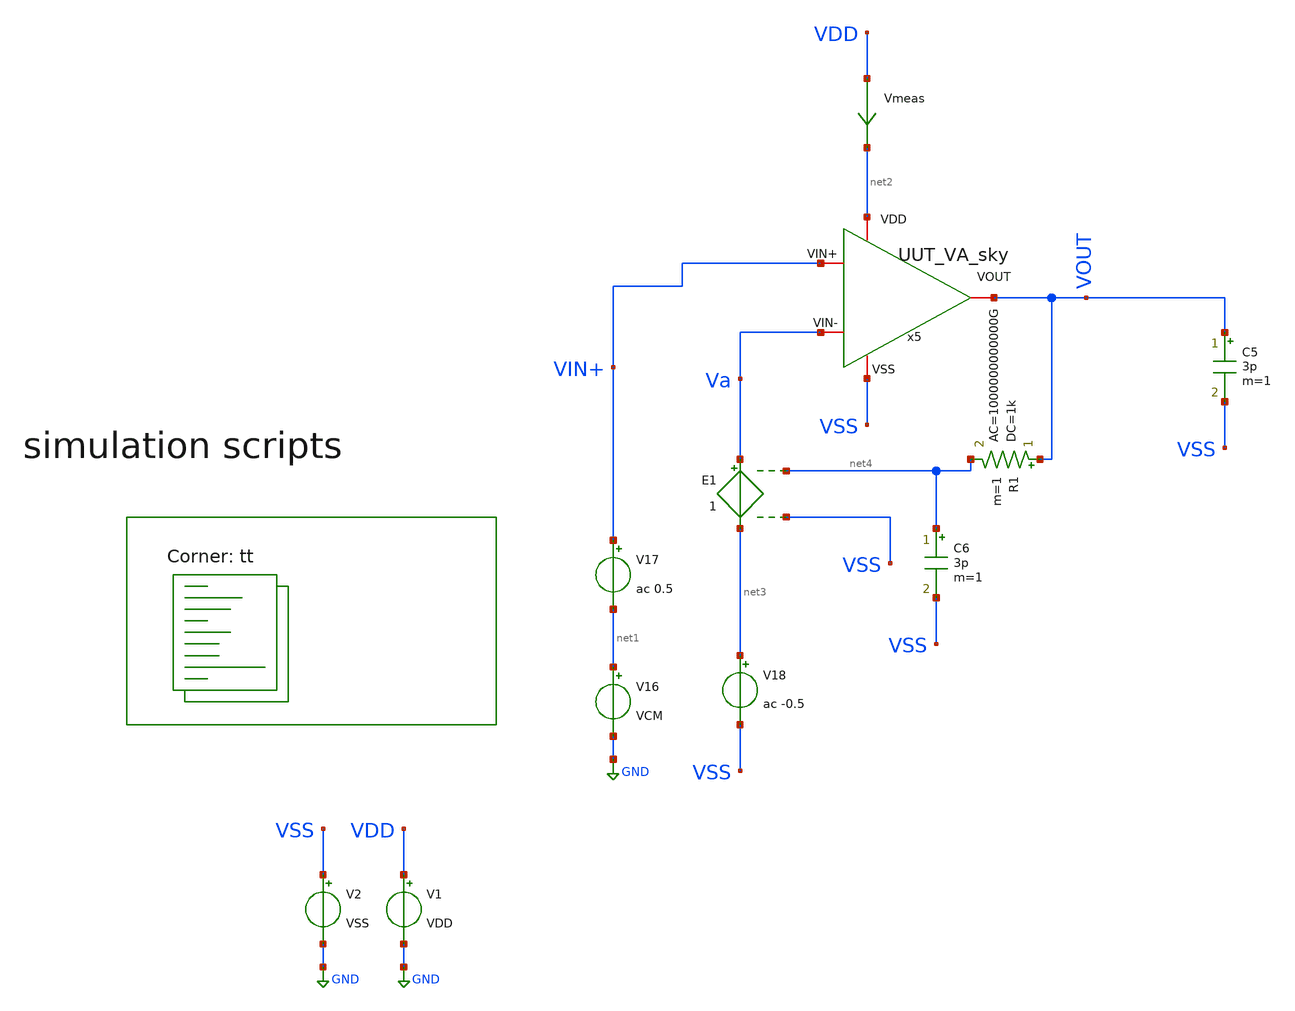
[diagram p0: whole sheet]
** sch_path: Learning/single_ended_amplifiers/VA001_series/Design_and_Analysis_of_Two-Stage_CMOS_Operational_Amplifier_for_Fluorescence_Signal_Processing_sky130_5V/amplifier_design/pz.sch
**.subckt pz
V1 VDD GND VDD
V2 VSS GND VSS
Vmeas VDD net2 0
.save i(vmeas)
x5 net2 VSS Va VIN+ VOUT UUT_VA_sky
C5 VOUT VSS 3p m=1
V16 net1 GND VCM
V17 VIN+ net1 ac 0.5
V18 net3 VSS ac -0.5
E1 Va net3 net4 VSS 1
R1 VOUT net4 1k ac=1000000000000G m=1
C6 net4 VSS 3p m=1
**** begin user architecture code
.lib $::SKYWATER_MODELS/sky130.lib.spice tt

.Temp 27
.param VDD = 5
.param VSS = 0
.param CL = 3p
.param V_OFF = -889u
.param VCM=2.5


.control
	save all
	ac dec 100 1 10G
	plot db(v(VOUT)) (180+(180*ph(v(VOUT))/pi))
	pz VIN+ 0 0 VOUT vol pz
	print all
.endc




**** end user architecture code
**.ends

* expanding   symbol:  Sky130A/UUT_sky/UUT_VA_sky.sym # of pins=5
** sym_path: my_ip/LIB/Sky130A/UUT_sky/UUT_VA_sky.sym
** sch_path: my_ip/LIB/Sky130A/UUT_sky/UUT_VA_sky.sch
.subckt UUT_VA_sky VDD VSS VIN- VIN+ VOUT
*.iopin VDD
*.iopin VSS
*.iopin VIN-
*.iopin VIN+
*.iopin VOUT
x1 VDD VSS VIN+ VIN- VOUT amplifier
.ends


* expanding   symbol:
*+  Sky130A/Learning/Design_of_Two-Stage_CMOS_Operational_Amplifier_for_Fluorescence_Signal_Processing_5V/amplifier.sym # of pins=5
** sym_path: my_ip/LIB/Sky130A/Learning/Design_of_Two-Stage_CMOS_Operational_Amplifier_for_Fluorescence_Signal_Processing_5V/amplifier.sym
** sch_path: my_ip/LIB/Sky130A/Learning/Design_of_Two-Stage_CMOS_Operational_Amplifier_for_Fluorescence_Signal_Processing_5V/amplifier.sch
.subckt amplifier VDD VSS Vin+ Vin- VOUT
*.iopin VDD
*.iopin VSS
*.iopin Vin+
*.iopin Vin-
*.iopin VOUT
XR2 VSS net2 VSS sky130_fd_pr__res_high_po_0p35 L=20.4 mult=1 m=1
XM7 net1 net1 VSS VSS sky130_fd_pr__nfet_g5v0d10v5 L=3.2 W='1 * 2 ' nf=2 ad='int((nf+1)/2) * W / nf * 0.29'
+ as='int((nf+2)/2) * W / nf * 0.29' pd='2*int((nf+1)/2) * (W / nf + 0.29)' ps='2*int((nf+2)/2) * (W / nf + 0.29)'
+ nrd='0.29 / W ' nrs='0.29 / W ' sa=0 sb=0 sd=0 mult=2 m=2
XM8 net3 net1 net2 VSS sky130_fd_pr__nfet_g5v0d10v5 L=3.2 W='1 * 8 ' nf=8 ad='int((nf+1)/2) * W / nf * 0.29'
+ as='int((nf+2)/2) * W / nf * 0.29' pd='2*int((nf+1)/2) * (W / nf + 0.29)' ps='2*int((nf+2)/2) * (W / nf + 0.29)'
+ nrd='0.29 / W ' nrs='0.29 / W ' sa=0 sb=0 sd=0 mult=2 m=2
XM9 VB1 VB2 net3 VSS sky130_fd_pr__nfet_g5v0d10v5 L=2 W='1 * 2 ' nf=2 ad='int((nf+1)/2) * W / nf * 0.29'
+ as='int((nf+2)/2) * W / nf * 0.29' pd='2*int((nf+1)/2) * (W / nf + 0.29)' ps='2*int((nf+2)/2) * (W / nf + 0.29)'
+ nrd='0.29 / W ' nrs='0.29 / W ' sa=0 sb=0 sd=0 mult=2 m=2
XM10 VB2 VB2 net1 VSS sky130_fd_pr__nfet_g5v0d10v5 L=2 W='1 * 2 ' nf=2 ad='int((nf+1)/2) * W / nf * 0.29'
+ as='int((nf+2)/2) * W / nf * 0.29' pd='2*int((nf+1)/2) * (W / nf + 0.29)' ps='2*int((nf+2)/2) * (W / nf + 0.29)'
+ nrd='0.29 / W ' nrs='0.29 / W ' sa=0 sb=0 sd=0 mult=2 m=2
XM2 net6 Vin- net4 net4 sky130_fd_pr__pfet_g5v0d10v5 L=1 W='4.5 * 2 ' nf=2 ad='int((2 + 1)/2) * 4.5 * 0.29'
+ as='int((2 + 2)/2) * 4.5 * 0.29' pd='2*int((2 + 1)/2) * (4.5 + 0.29)' ps='2*int((2 + 2)/2) * (4.5 + 0.29)'
+ nrd='0.29 / 4.5 / 2 ' nrs='0.29 / 4.5 / 2 ' sa=0 sb=0 sd=0 mult=4 m=4
XM3 net5 Vin+ net4 net4 sky130_fd_pr__pfet_g5v0d10v5 L=1 W='4.5 * 2 ' nf=2 ad='int((2 + 1)/2) * 4.5 * 0.29'
+ as='int((2 + 2)/2) * 4.5 * 0.29' pd='2*int((2 + 1)/2) * (4.5 + 0.29)' ps='2*int((2 + 2)/2) * (4.5 + 0.29)'
+ nrd='0.29 / 4.5 / 2 ' nrs='0.29 / 4.5 / 2 ' sa=0 sb=0 sd=0 mult=4 m=4
XM4 net5 net6 VSS VSS sky130_fd_pr__nfet_g5v0d10v5 L=2 W='1.5 * 2 ' nf=2 ad='int((nf+1)/2) * W / nf * 0.29'
+ as='int((nf+2)/2) * W / nf * 0.29' pd='2*int((nf+1)/2) * (W / nf + 0.29)' ps='2*int((nf+2)/2) * (W / nf + 0.29)'
+ nrd='0.29 / W ' nrs='0.29 / W ' sa=0 sb=0 sd=0 mult=2 m=2
XM11 net6 net6 VSS VSS sky130_fd_pr__nfet_g5v0d10v5 L=2 W='1.5 * 2 ' nf=2 ad='int((nf+1)/2) * W / nf * 0.29'
+ as='int((nf+2)/2) * W / nf * 0.29' pd='2*int((nf+1)/2) * (W / nf + 0.29)' ps='2*int((nf+2)/2) * (W / nf + 0.29)'
+ nrd='0.29 / W ' nrs='0.29 / W ' sa=0 sb=0 sd=0 mult=2 m=2
XM13 VOUT net5 VSS VSS sky130_fd_pr__nfet_g5v0d10v5 L=1 W='4 * 2 ' nf=2 ad='int((nf+1)/2) * W / nf * 0.29'
+ as='int((nf+2)/2) * W / nf * 0.29' pd='2*int((nf+1)/2) * (W / nf + 0.29)' ps='2*int((nf+2)/2) * (W / nf + 0.29)'
+ nrd='0.29 / W ' nrs='0.29 / W ' sa=0 sb=0 sd=0 mult=2 m=2
XM14 net7 VB2 net5 VSS sky130_fd_pr__nfet_g5v0d10v5 L=2 W='1.4 * 1 ' nf=1 ad='int((nf+1)/2) * W / nf * 0.29'
+ as='int((nf+2)/2) * W / nf * 0.29' pd='2*int((nf+1)/2) * (W / nf + 0.29)' ps='2*int((nf+2)/2) * (W / nf + 0.29)'
+ nrd='0.29 / W ' nrs='0.29 / W ' sa=0 sb=0 sd=0 mult=2 m=2
XC1 VOUT net7 sky130_fd_pr__cap_mim_m3_1 W=8 L=8 MF=4 m=4
XM1 VB2 VB1 VDD VDD sky130_fd_pr__pfet_g5v0d10v5 L=2.2 W='1 * 2 ' nf=2 ad='int((2 + 1)/2) * 1 * 0.29'
+ as='int((2 + 2)/2) * 1 * 0.29' pd='2*int((2 + 1)/2) * (1 + 0.29)' ps='2*int((2 + 2)/2) * (1 + 0.29)'
+ nrd='0.29 / 1 / 2 ' nrs='0.29 / 1 / 2 ' sa=0 sb=0 sd=0 mult=2 m=2
XM5 VB1 VB1 VDD VDD sky130_fd_pr__pfet_g5v0d10v5 L=2.2 W='1 * 2 ' nf=2 ad='int((2 + 1)/2) * 1 * 0.29'
+ as='int((2 + 2)/2) * 1 * 0.29' pd='2*int((2 + 1)/2) * (1 + 0.29)' ps='2*int((2 + 2)/2) * (1 + 0.29)'
+ nrd='0.29 / 1 / 2 ' nrs='0.29 / 1 / 2 ' sa=0 sb=0 sd=0 mult=2 m=2
XM6 net4 VB1 VDD VDD sky130_fd_pr__pfet_g5v0d10v5 L=2.2 W='1 * 2 ' nf=2 ad='int((2 + 1)/2) * 1 * 0.29'
+ as='int((2 + 2)/2) * 1 * 0.29' pd='2*int((2 + 1)/2) * (1 + 0.29)' ps='2*int((2 + 2)/2) * (1 + 0.29)'
+ nrd='0.29 / 1 / 2 ' nrs='0.29 / 1 / 2 ' sa=0 sb=0 sd=0 mult=8 m=8
XM12 VOUT VB1 VDD VDD sky130_fd_pr__pfet_g5v0d10v5 L=2.2 W='1 * 2 ' nf=2 ad='int((2 + 1)/2) * 1 * 0.29'
+ as='int((2 + 2)/2) * 1 * 0.29' pd='2*int((2 + 1)/2) * (1 + 0.29)' ps='2*int((2 + 2)/2) * (1 + 0.29)'
+ nrd='0.29 / 1 / 2 ' nrs='0.29 / 1 / 2 ' sa=0 sb=0 sd=0 mult=16 m=16
.ends

.GLOBAL GND
.end
